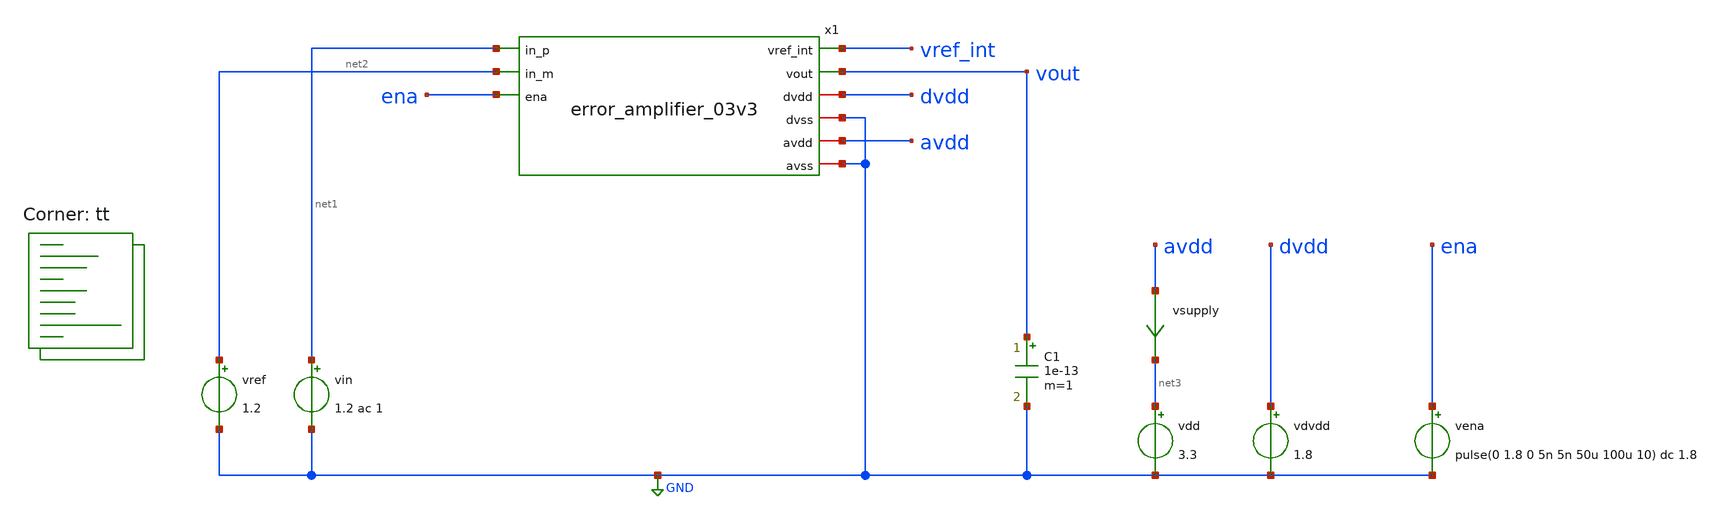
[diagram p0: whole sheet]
** sch_path: xschem/error_amplifier_03v3_tb.sch
**.subckt error_amplifier_03v3_tb
vdd net3 GND 3.3
vsupply avdd net3 0
.save i(vsupply)
C1 vout GND 1e-13 m=1
vena ena GND pulse(0 1.8 0 5n 5n 50u 100u 10) dc 1.8
vdvdd dvdd GND 1.8
x1 vref_int net1 vout net2 ena dvdd GND avdd GND error_amplifier_03v3
vref net2 GND 1.2
vin net1 GND 1.2 ac 1
**** begin user architecture code

* ngspice control
.param W=100
.option savecurrents
.control
save all
op
write error_amplifier_03v3_tb.raw
set appendwrite

dc vdd 0 3.3 10m
plot vout title 'Vdd operating range'

* tran 100n 100u
* plot x1.vbn x1.vcp x1.vbp ena x1.ena_3v3 title 'Transient start-up'
* plot ena x1.ena_b x1.ena_3v3 x1.ena_b_3v3

dc vin 0 3.3 10m
plot vout title 'DC transfer characteristic'

ac dec 10 10 1e9
set units=degrees
plot db(vout) title 'Gain'
plot ph(vout) title 'Phase'
.endc


.lib $::SKYWATER_MODELS/sky130.lib.spice tt
**** end user architecture code
**.ends

* expanding   symbol:  error_amplifier_03v3.sym # of pins=9
** sym_path: xschem/error_amplifier_03v3.sym
** sch_path: xschem/error_amplifier_03v3.sch
.subckt error_amplifier_03v3 vref_int in_p vout in_m ena dvdd dvss avdd avss
*.ipin in_m
*.ipin in_p
*.opin vout
*.ipin ena
*.opin vref_int
*.iopin dvdd
*.iopin dvss
*.iopin avdd
*.iopin avss
XM1 vbn vbn avss avss sky130_fd_pr__nfet_g5v0d10v5 L=10 W=1 nf=1 ad='int((nf+1)/2) * W/nf * 0.29' as='int((nf+2)/2) * W/nf * 0.29'
+ pd='2*int((nf+1)/2) * (W/nf + 0.29)' ps='2*int((nf+2)/2) * (W/nf + 0.29)' nrd='0.29 / W' nrs='0.29 / W'
+ sa=0 sb=0 sd=0 mult=1 m=1
XM3 vcp vbn net6 avss sky130_fd_pr__nfet_g5v0d10v5 L=10 W=1 nf=1 ad='int((nf+1)/2) * W/nf * 0.29' as='int((nf+2)/2) * W/nf * 0.29'
+ pd='2*int((nf+1)/2) * (W/nf + 0.29)' ps='2*int((nf+2)/2) * (W/nf + 0.29)' nrd='0.29 / W' nrs='0.29 / W'
+ sa=0 sb=0 sd=0 mult=4 m=4
XM5 vbp vbp avdd avdd sky130_fd_pr__pfet_g5v0d10v5 L=10 W=1 nf=1 ad='int((nf+1)/2) * W/nf * 0.29' as='int((nf+2)/2) * W/nf * 0.29'
+ pd='2*int((nf+1)/2) * (W/nf + 0.29)' ps='2*int((nf+2)/2) * (W/nf + 0.29)' nrd='0.29 / W' nrs='0.29 / W'
+ sa=0 sb=0 sd=0 mult=2 m=2
XM26 net4 vbp avdd avdd sky130_fd_pr__pfet_g5v0d10v5 L=10 W=1 nf=1 ad='int((nf+1)/2) * W/nf * 0.29' as='int((nf+2)/2) * W/nf * 0.29'
+ pd='2*int((nf+1)/2) * (W/nf + 0.29)' ps='2*int((nf+2)/2) * (W/nf + 0.29)' nrd='0.29 / W' nrs='0.29 / W'
+ sa=0 sb=0 sd=0 mult=6 m=6
XM27 net5 vbp avdd avdd sky130_fd_pr__pfet_g5v0d10v5 L=10 W=1 nf=1 ad='int((nf+1)/2) * W/nf * 0.29' as='int((nf+2)/2) * W/nf * 0.29'
+ pd='2*int((nf+1)/2) * (W/nf + 0.29)' ps='2*int((nf+2)/2) * (W/nf + 0.29)' nrd='0.29 / W' nrs='0.29 / W'
+ sa=0 sb=0 sd=0 mult=6 m=6
XM28 net3 vcp net4 avdd sky130_fd_pr__pfet_g5v0d10v5 L=2 W=1 nf=1 ad='int((nf+1)/2) * W/nf * 0.29' as='int((nf+2)/2) * W/nf * 0.29'
+ pd='2*int((nf+1)/2) * (W/nf + 0.29)' ps='2*int((nf+2)/2) * (W/nf + 0.29)' nrd='0.29 / W' nrs='0.29 / W'
+ sa=0 sb=0 sd=0 mult=1 m=1
XM29 v_cascode vcp net5 avdd sky130_fd_pr__pfet_g5v0d10v5 L=2 W=1 nf=1 ad='int((nf+1)/2) * W/nf * 0.29'
+ as='int((nf+2)/2) * W/nf * 0.29' pd='2*int((nf+1)/2) * (W/nf + 0.29)' ps='2*int((nf+2)/2) * (W/nf + 0.29)'
+ nrd='0.29 / W' nrs='0.29 / W' sa=0 sb=0 sd=0 mult=1 m=1
XM30 net3 vcn net1 avss sky130_fd_pr__nfet_g5v0d10v5 L=2 W=1 nf=1 ad='int((nf+1)/2) * W/nf * 0.29' as='int((nf+2)/2) * W/nf * 0.29'
+ pd='2*int((nf+1)/2) * (W/nf + 0.29)' ps='2*int((nf+2)/2) * (W/nf + 0.29)' nrd='0.29 / W' nrs='0.29 / W'
+ sa=0 sb=0 sd=0 mult=1 m=1
XM31 v_cascode vcn net2 avss sky130_fd_pr__nfet_g5v0d10v5 L=2 W=1 nf=1 ad='int((nf+1)/2) * W/nf * 0.29'
+ as='int((nf+2)/2) * W/nf * 0.29' pd='2*int((nf+1)/2) * (W/nf + 0.29)' ps='2*int((nf+2)/2) * (W/nf + 0.29)'
+ nrd='0.29 / W' nrs='0.29 / W' sa=0 sb=0 sd=0 mult=1 m=1
XM32 net1 net3 avss avss sky130_fd_pr__nfet_g5v0d10v5 L=10 W=1 nf=1 ad='int((nf+1)/2) * W/nf * 0.29'
+ as='int((nf+2)/2) * W/nf * 0.29' pd='2*int((nf+1)/2) * (W/nf + 0.29)' ps='2*int((nf+2)/2) * (W/nf + 0.29)'
+ nrd='0.29 / W' nrs='0.29 / W' sa=0 sb=0 sd=0 mult=3 m=3
XM33 net2 net3 avss avss sky130_fd_pr__nfet_g5v0d10v5 L=10 W=1 nf=1 ad='int((nf+1)/2) * W/nf * 0.29'
+ as='int((nf+2)/2) * W/nf * 0.29' pd='2*int((nf+1)/2) * (W/nf + 0.29)' ps='2*int((nf+2)/2) * (W/nf + 0.29)'
+ nrd='0.29 / W' nrs='0.29 / W' sa=0 sb=0 sd=0 mult=3 m=3
XM35 net11 vbp avdd avdd sky130_fd_pr__pfet_g5v0d10v5 L=10 W=1 nf=1 ad='int((nf+1)/2) * W/nf * 0.29'
+ as='int((nf+2)/2) * W/nf * 0.29' pd='2*int((nf+1)/2) * (W/nf + 0.29)' ps='2*int((nf+2)/2) * (W/nf + 0.29)'
+ nrd='0.29 / W' nrs='0.29 / W' sa=0 sb=0 sd=0 mult=2 m=2
XR3 avss net6 avss sky130_fd_pr__res_xhigh_po_0p35 L=180 mult=1 m=1
XM9 net12 v_cascode vout avdd sky130_fd_pr__pfet_g5v0d10v5 L=10 W=1 nf=1 ad='int((nf+1)/2) * W/nf * 0.29'
+ as='int((nf+2)/2) * W/nf * 0.29' pd='2*int((nf+1)/2) * (W/nf + 0.29)' ps='2*int((nf+2)/2) * (W/nf + 0.29)'
+ nrd='0.29 / W' nrs='0.29 / W' sa=0 sb=0 sd=0 mult=1 m=1
XM8 vout vbp avdd avdd sky130_fd_pr__pfet_g5v0d10v5 L=10 W=1 nf=1 ad='int((nf+1)/2) * W/nf * 0.29' as='int((nf+2)/2) * W/nf * 0.29'
+ pd='2*int((nf+1)/2) * (W/nf + 0.29)' ps='2*int((nf+2)/2) * (W/nf + 0.29)' nrd='0.29 / W' nrs='0.29 / W'
+ sa=0 sb=0 sd=0 mult=10 m=10
XM17 net8 vbp avdd avdd sky130_fd_pr__pfet_g5v0d10v5 L=10 W=1 nf=1 ad='int((nf+1)/2) * W/nf * 0.29' as='int((nf+2)/2) * W/nf * 0.29'
+ pd='2*int((nf+1)/2) * (W/nf + 0.29)' ps='2*int((nf+2)/2) * (W/nf + 0.29)' nrd='0.29 / W' nrs='0.29 / W'
+ sa=0 sb=0 sd=0 mult=1 m=1
XM19 net8 net8 net7 avss sky130_fd_pr__nfet_g5v0d10v5 L=0.5 W=1 nf=1 ad='int((nf+1)/2) * W/nf * 0.29'
+ as='int((nf+2)/2) * W/nf * 0.29' pd='2*int((nf+1)/2) * (W/nf + 0.29)' ps='2*int((nf+2)/2) * (W/nf + 0.29)'
+ nrd='0.29 / W' nrs='0.29 / W' sa=0 sb=0 sd=0 mult=6 m=6
XM20 net7 net8 avss avss sky130_fd_pr__nfet_g5v0d10v5 L=0.5 W=1 nf=1 ad='int((nf+1)/2) * W/nf * 0.29'
+ as='int((nf+2)/2) * W/nf * 0.29' pd='2*int((nf+1)/2) * (W/nf + 0.29)' ps='2*int((nf+2)/2) * (W/nf + 0.29)'
+ nrd='0.29 / W' nrs='0.29 / W' sa=0 sb=0 sd=0 mult=1 m=1
XM21 vcn vbp avdd avdd sky130_fd_pr__pfet_g5v0d10v5 L=10 W=1 nf=1 ad='int((nf+1)/2) * W/nf * 0.29' as='int((nf+2)/2) * W/nf * 0.29'
+ pd='2*int((nf+1)/2) * (W/nf + 0.29)' ps='2*int((nf+2)/2) * (W/nf + 0.29)' nrd='0.29 / W' nrs='0.29 / W'
+ sa=0 sb=0 sd=0 mult=5 m=5
XM36 vcn vcn net7 avss sky130_fd_pr__nfet_g5v0d10v5 L=2 W=1 nf=1 ad='int((nf+1)/2) * W/nf * 0.29' as='int((nf+2)/2) * W/nf * 0.29'
+ pd='2*int((nf+1)/2) * (W/nf + 0.29)' ps='2*int((nf+2)/2) * (W/nf + 0.29)' nrd='0.29 / W' nrs='0.29 / W'
+ sa=0 sb=0 sd=0 mult=1 m=1
XM6 net5 in_m net9 avss sky130_fd_pr__nfet_g5v0d10v5 L=0.5 W=1 nf=1 ad='int((nf+1)/2) * W/nf * 0.29'
+ as='int((nf+2)/2) * W/nf * 0.29' pd='2*int((nf+1)/2) * (W/nf + 0.29)' ps='2*int((nf+2)/2) * (W/nf + 0.29)'
+ nrd='0.29 / W' nrs='0.29 / W' sa=0 sb=0 sd=0 mult=1 m=1
XM7 net9 vbn avss avss sky130_fd_pr__nfet_g5v0d10v5 L=10 W=1 nf=1 ad='int((nf+1)/2) * W/nf * 0.29' as='int((nf+2)/2) * W/nf * 0.29'
+ pd='2*int((nf+1)/2) * (W/nf + 0.29)' ps='2*int((nf+2)/2) * (W/nf + 0.29)' nrd='0.29 / W' nrs='0.29 / W'
+ sa=0 sb=0 sd=0 mult=2 m=2
XM12 net4 in_p net9 avss sky130_fd_pr__nfet_g5v0d10v5 L=0.5 W=1 nf=1 ad='int((nf+1)/2) * W/nf * 0.29'
+ as='int((nf+2)/2) * W/nf * 0.29' pd='2*int((nf+1)/2) * (W/nf + 0.29)' ps='2*int((nf+2)/2) * (W/nf + 0.29)'
+ nrd='0.29 / W' nrs='0.29 / W' sa=0 sb=0 sd=0 mult=1 m=1
XM10 vstart vbn avss avss sky130_fd_pr__nfet_g5v0d10v5 L=1 W=10 nf=1 ad='int((nf+1)/2) * W/nf * 0.29'
+ as='int((nf+2)/2) * W/nf * 0.29' pd='2*int((nf+1)/2) * (W/nf + 0.29)' ps='2*int((nf+2)/2) * (W/nf + 0.29)'
+ nrd='0.29 / W' nrs='0.29 / W' sa=0 sb=0 sd=0 mult=1 m=1
XM11 vstart avss net10 avdd sky130_fd_pr__pfet_g5v0d10v5 L=20 W=1 nf=1 ad='int((nf+1)/2) * W/nf * 0.29'
+ as='int((nf+2)/2) * W/nf * 0.29' pd='2*int((nf+1)/2) * (W/nf + 0.29)' ps='2*int((nf+2)/2) * (W/nf + 0.29)'
+ nrd='0.29 / W' nrs='0.29 / W' sa=0 sb=0 sd=0 mult=1 m=1
XM2 vcp vcp vbp avdd sky130_fd_pr__pfet_g5v0d10v5 L=10 W=1 nf=1 ad='int((nf+1)/2) * W/nf * 0.29' as='int((nf+2)/2) * W/nf * 0.29'
+ pd='2*int((nf+1)/2) * (W/nf + 0.29)' ps='2*int((nf+2)/2) * (W/nf + 0.29)' nrd='0.29 / W' nrs='0.29 / W'
+ sa=0 sb=0 sd=0 mult=2 m=2
XM4 vbn vcp net11 avdd sky130_fd_pr__pfet_g5v0d10v5 L=10 W=1 nf=1 ad='int((nf+1)/2) * W/nf * 0.29' as='int((nf+2)/2) * W/nf * 0.29'
+ pd='2*int((nf+1)/2) * (W/nf + 0.29)' ps='2*int((nf+2)/2) * (W/nf + 0.29)' nrd='0.29 / W' nrs='0.29 / W'
+ sa=0 sb=0 sd=0 mult=2 m=2
XM13 vbp vstart avss avss sky130_fd_pr__nfet_g5v0d10v5 L=0.5 W=1 nf=1 ad='int((nf+1)/2) * W/nf * 0.29'
+ as='int((nf+2)/2) * W/nf * 0.29' pd='2*int((nf+1)/2) * (W/nf + 0.29)' ps='2*int((nf+2)/2) * (W/nf + 0.29)'
+ nrd='0.29 / W' nrs='0.29 / W' sa=0 sb=0 sd=0 mult=1 m=1
XM14 vcp vstart avss avss sky130_fd_pr__nfet_g5v0d10v5 L=0.5 W=1 nf=1 ad='int((nf+1)/2) * W/nf * 0.29'
+ as='int((nf+2)/2) * W/nf * 0.29' pd='2*int((nf+1)/2) * (W/nf + 0.29)' ps='2*int((nf+2)/2) * (W/nf + 0.29)'
+ nrd='0.29 / W' nrs='0.29 / W' sa=0 sb=0 sd=0 mult=1 m=1
XM15 net10 net10 vstart_supply avdd sky130_fd_pr__pfet_g5v0d10v5 L=20 W=1 nf=1 ad='int((nf+1)/2) * W/nf * 0.29'
+ as='int((nf+2)/2) * W/nf * 0.29' pd='2*int((nf+1)/2) * (W/nf + 0.29)' ps='2*int((nf+2)/2) * (W/nf + 0.29)'
+ nrd='0.29 / W' nrs='0.29 / W' sa=0 sb=0 sd=0 mult=1 m=1
XM16 vbp ena_3v3 avdd avdd sky130_fd_pr__pfet_g5v0d10v5 L=0.5 W=1 nf=1 ad='int((nf+1)/2) * W/nf * 0.29'
+ as='int((nf+2)/2) * W/nf * 0.29' pd='2*int((nf+1)/2) * (W/nf + 0.29)' ps='2*int((nf+2)/2) * (W/nf + 0.29)'
+ nrd='0.29 / W' nrs='0.29 / W' sa=0 sb=0 sd=0 mult=1 m=1
XM18 vcp ena_3v3 avdd avdd sky130_fd_pr__pfet_g5v0d10v5 L=0.5 W=1 nf=1 ad='int((nf+1)/2) * W/nf * 0.29'
+ as='int((nf+2)/2) * W/nf * 0.29' pd='2*int((nf+1)/2) * (W/nf + 0.29)' ps='2*int((nf+2)/2) * (W/nf + 0.29)'
+ nrd='0.29 / W' nrs='0.29 / W' sa=0 sb=0 sd=0 mult=1 m=1
XM22 vbn ena_b_3v3 avss avss sky130_fd_pr__nfet_g5v0d10v5 L=0.5 W=1 nf=1 ad='int((nf+1)/2) * W/nf * 0.29'
+ as='int((nf+2)/2) * W/nf * 0.29' pd='2*int((nf+1)/2) * (W/nf + 0.29)' ps='2*int((nf+2)/2) * (W/nf + 0.29)'
+ nrd='0.29 / W' nrs='0.29 / W' sa=0 sb=0 sd=0 mult=1 m=1
XM23 vcn ena_b_3v3 avss avss sky130_fd_pr__nfet_g5v0d10v5 L=0.5 W=1 nf=1 ad='int((nf+1)/2) * W/nf * 0.29'
+ as='int((nf+2)/2) * W/nf * 0.29' pd='2*int((nf+1)/2) * (W/nf + 0.29)' ps='2*int((nf+2)/2) * (W/nf + 0.29)'
+ nrd='0.29 / W' nrs='0.29 / W' sa=0 sb=0 sd=0 mult=1 m=1
XM24 v_cascode ena_b_3v3 avss avss sky130_fd_pr__nfet_g5v0d10v5 L=0.5 W=1 nf=1 ad='int((nf+1)/2) * W/nf * 0.29'
+ as='int((nf+2)/2) * W/nf * 0.29' pd='2*int((nf+1)/2) * (W/nf + 0.29)' ps='2*int((nf+2)/2) * (W/nf + 0.29)'
+ nrd='0.29 / W' nrs='0.29 / W' sa=0 sb=0 sd=0 mult=1 m=1
XM25 out ena_b_3v3 avss avss sky130_fd_pr__nfet_g5v0d10v5 L=0.5 W=1 nf=1 ad='int((nf+1)/2) * W/nf * 0.29'
+ as='int((nf+2)/2) * W/nf * 0.29' pd='2*int((nf+1)/2) * (W/nf + 0.29)' ps='2*int((nf+2)/2) * (W/nf + 0.29)'
+ nrd='0.29 / W' nrs='0.29 / W' sa=0 sb=0 sd=0 mult=1 m=1
XM34 vstart ena_b_3v3 avss avss sky130_fd_pr__nfet_g5v0d10v5 L=0.5 W=1 nf=1 ad='int((nf+1)/2) * W/nf * 0.29'
+ as='int((nf+2)/2) * W/nf * 0.29' pd='2*int((nf+1)/2) * (W/nf + 0.29)' ps='2*int((nf+2)/2) * (W/nf + 0.29)'
+ nrd='0.29 / W' nrs='0.29 / W' sa=0 sb=0 sd=0 mult=1 m=1
XM38 net12 vbn avss avss sky130_fd_pr__nfet_g5v0d10v5 L=10 W=1 nf=1 ad='int((nf+1)/2) * W/nf * 0.29'
+ as='int((nf+2)/2) * W/nf * 0.29' pd='2*int((nf+1)/2) * (W/nf + 0.29)' ps='2*int((nf+2)/2) * (W/nf + 0.29)'
+ nrd='0.29 / W' nrs='0.29 / W' sa=0 sb=0 sd=0 mult=2 m=2
XM39 vout net12 avss avss sky130_fd_pr__nfet_g5v0d10v5 L=0.5 W=4 nf=1 ad='int((nf+1)/2) * W/nf * 0.29'
+ as='int((nf+2)/2) * W/nf * 0.29' pd='2*int((nf+1)/2) * (W/nf + 0.29)' ps='2*int((nf+2)/2) * (W/nf + 0.29)'
+ nrd='0.29 / W' nrs='0.29 / W' sa=0 sb=0 sd=0 mult=1 m=1
XM43 ena_b_3v3 ena_3v3 avdd avdd sky130_fd_pr__pfet_g5v0d10v5 L=1 W=1 nf=1 ad='int((nf+1)/2) * W/nf * 0.29'
+ as='int((nf+2)/2) * W/nf * 0.29' pd='2*int((nf+1)/2) * (W/nf + 0.29)' ps='2*int((nf+2)/2) * (W/nf + 0.29)'
+ nrd='0.29 / W' nrs='0.29 / W' sa=0 sb=0 sd=0 mult=1 m=1
XM44 ena_b_3v3 ena avss avss sky130_fd_pr__nfet_g5v0d10v5 L=0.5 W=1 nf=1 ad='int((nf+1)/2) * W/nf * 0.29'
+ as='int((nf+2)/2) * W/nf * 0.29' pd='2*int((nf+1)/2) * (W/nf + 0.29)' ps='2*int((nf+2)/2) * (W/nf + 0.29)'
+ nrd='0.29 / W' nrs='0.29 / W' sa=0 sb=0 sd=0 mult=1 m=1
XM45 ena_3v3 ena_b_3v3 avdd avdd sky130_fd_pr__pfet_g5v0d10v5 L=1 W=1 nf=1 ad='int((nf+1)/2) * W/nf * 0.29'
+ as='int((nf+2)/2) * W/nf * 0.29' pd='2*int((nf+1)/2) * (W/nf + 0.29)' ps='2*int((nf+2)/2) * (W/nf + 0.29)'
+ nrd='0.29 / W' nrs='0.29 / W' sa=0 sb=0 sd=0 mult=1 m=1
XM46 ena_3v3 ena_b avss avss sky130_fd_pr__nfet_g5v0d10v5 L=0.5 W=1 nf=1 ad='int((nf+1)/2) * W/nf * 0.29'
+ as='int((nf+2)/2) * W/nf * 0.29' pd='2*int((nf+1)/2) * (W/nf + 0.29)' ps='2*int((nf+2)/2) * (W/nf + 0.29)'
+ nrd='0.29 / W' nrs='0.29 / W' sa=0 sb=0 sd=0 mult=1 m=1
XC1 vout v_cascode sky130_fd_pr__cap_mim_m3_1 W=6 L=6 MF=4 m=4
XM40 vref_int vbp avdd avdd sky130_fd_pr__pfet_g5v0d10v5 L=10 W=1 nf=1 ad='int((nf+1)/2) * W/nf * 0.29'
+ as='int((nf+2)/2) * W/nf * 0.29' pd='2*int((nf+1)/2) * (W/nf + 0.29)' ps='2*int((nf+2)/2) * (W/nf + 0.29)'
+ nrd='0.29 / W' nrs='0.29 / W' sa=0 sb=0 sd=0 mult=15 m=15
XM47 vref_int vref_int avss avss sky130_fd_pr__nfet_g5v0d10v5 L=20 W=1.05 nf=1 ad='int((nf+1)/2) * W/nf * 0.29'
+ as='int((nf+2)/2) * W/nf * 0.29' pd='2*int((nf+1)/2) * (W/nf + 0.29)' ps='2*int((nf+2)/2) * (W/nf + 0.29)'
+ nrd='0.29 / W' nrs='0.29 / W' sa=0 sb=0 sd=0 mult=1 m=1
XM48 vstart_supply ena_b_3v3 avdd avdd sky130_fd_pr__pfet_g5v0d10v5 L=0.5 W=1 nf=1 ad='int((nf+1)/2) * W/nf * 0.29'
+ as='int((nf+2)/2) * W/nf * 0.29' pd='2*int((nf+1)/2) * (W/nf + 0.29)' ps='2*int((nf+2)/2) * (W/nf + 0.29)'
+ nrd='0.29 / W' nrs='0.29 / W' sa=0 sb=0 sd=0 mult=1 m=1
XM41 ena_b ena dvss dvss sky130_fd_pr__nfet_01v8 L=0.15 W=1 nf=1 ad='int((nf+1)/2) * W/nf * 0.29' as='int((nf+2)/2) * W/nf * 0.29'
+ pd='2*int((nf+1)/2) * (W/nf + 0.29)' ps='2*int((nf+2)/2) * (W/nf + 0.29)' nrd='0.29 / W' nrs='0.29 / W'
+ sa=0 sb=0 sd=0 mult=1 m=1
XM37 ena_b ena dvdd dvdd sky130_fd_pr__pfet_01v8 L=0.15 W=10 nf=1 ad='int((nf+1)/2) * W/nf * 0.29' as='int((nf+2)/2) * W/nf * 0.29'
+ pd='2*int((nf+1)/2) * (W/nf + 0.29)' ps='2*int((nf+2)/2) * (W/nf + 0.29)' nrd='0.29 / W' nrs='0.29 / W'
+ sa=0 sb=0 sd=0 mult=1 m=1
.ends

.GLOBAL GND
.end
